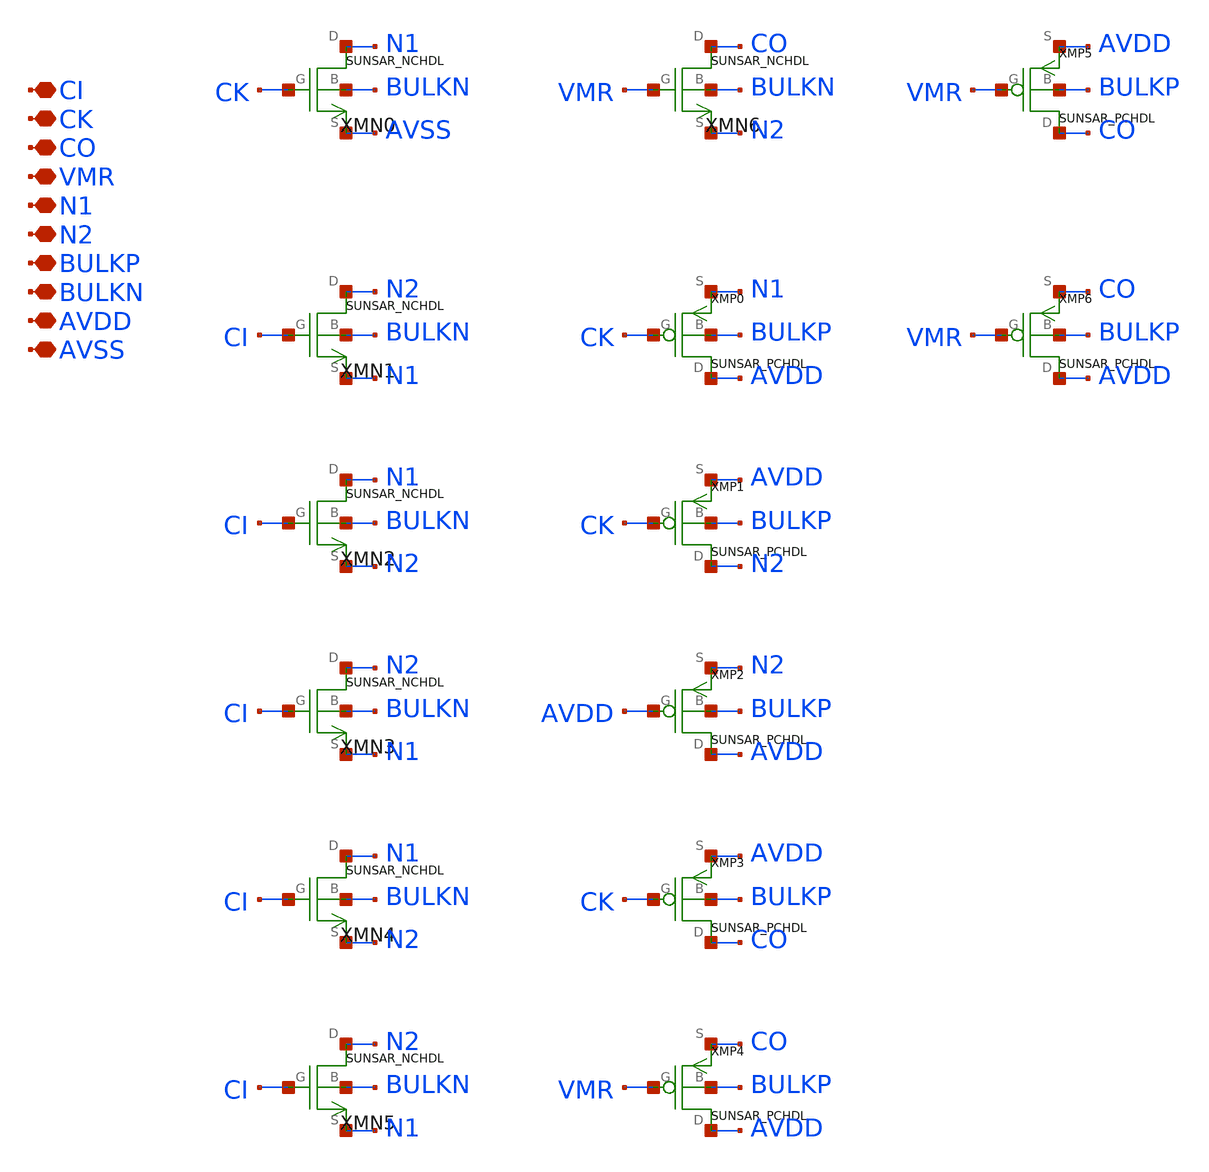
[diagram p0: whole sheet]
** sch_path: ip/sun_sar9b_sky130nm/design/SUN_SAR9B_SKY130NM/SUNSAR_SARCMPHX1_CV.sch
**.subckt SUNSAR_SARCMPHX1_CV CI CK CO VMR N1 N2 BULKP BULKN AVDD AVSS
*.iopin CI
*.iopin CK
*.iopin CO
*.iopin VMR
*.iopin N1
*.iopin N2
*.iopin BULKP
*.iopin BULKN
*.iopin AVDD
*.iopin AVSS
XMN0 N1 CK AVSS BULKN SUNSAR_NCHDL
XMN1 N2 CI N1 BULKN SUNSAR_NCHDL
XMN2 N1 CI N2 BULKN SUNSAR_NCHDL
XMN3 N2 CI N1 BULKN SUNSAR_NCHDL
XMN4 N1 CI N2 BULKN SUNSAR_NCHDL
XMN5 N2 CI N1 BULKN SUNSAR_NCHDL
XMN6 CO VMR N2 BULKN SUNSAR_NCHDL
XMP0 AVDD CK N1 BULKP SUNSAR_PCHDL
XMP1 N2 CK AVDD BULKP SUNSAR_PCHDL
XMP2 AVDD AVDD N2 BULKP SUNSAR_PCHDL
XMP3 CO CK AVDD BULKP SUNSAR_PCHDL
XMP4 AVDD VMR CO BULKP SUNSAR_PCHDL
XMP5 CO VMR AVDD BULKP SUNSAR_PCHDL
XMP6 AVDD VMR CO BULKP SUNSAR_PCHDL
**.ends
.end
